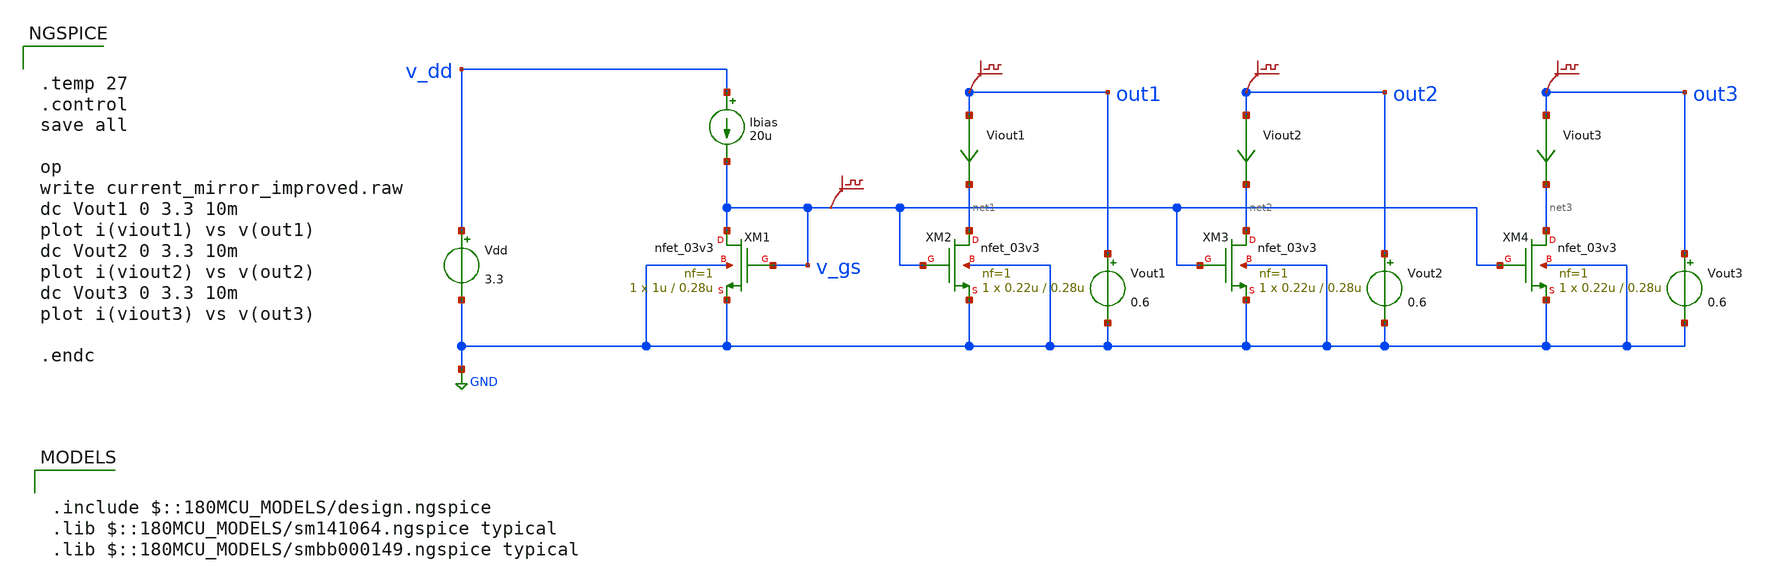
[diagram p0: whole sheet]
** sch_path: Modulo_Analogico/Laboratorios/Lab4/current_mirror_improved.sch
**.subckt current_mirror_improved
Vdd v_dd GND 3.3
Ibias v_dd v_gs 20u
Vout1 out1 GND 0.6
Vout2 out2 GND 0.6
Vout3 out3 GND 0.6
.save v(out1)
.save v(out2)
.save v(out3)
.save v(v_gs)
Viout1 out1 net1 0
.save i(viout1)
Viout2 out2 net2 0
.save i(viout2)
Viout3 out3 net3 0
.save i(viout3)
XM1 v_gs v_gs GND GND nfet_03v3 L=0.28u W=1u nf=1 ad='int((nf+1)/2) * W/nf * 0.18u' as='int((nf+2)/2) * W/nf * 0.18u'
+ pd='2*int((nf+1)/2) * (W/nf + 0.18u)' ps='2*int((nf+2)/2) * (W/nf + 0.18u)' nrd='0.18u / W' nrs='0.18u / W'
+ sa=0 sb=0 sd=0 m=1
XM2 net1 v_gs GND GND nfet_03v3 L=0.28u W=0.22u nf=1 ad='int((nf+1)/2) * W/nf * 0.18u' as='int((nf+2)/2) * W/nf * 0.18u'
+ pd='2*int((nf+1)/2) * (W/nf + 0.18u)' ps='2*int((nf+2)/2) * (W/nf + 0.18u)' nrd='0.18u / W' nrs='0.18u / W'
+ sa=0 sb=0 sd=0 m=1
XM3 net2 v_gs GND GND nfet_03v3 L=0.28u W=0.22u nf=1 ad='int((nf+1)/2) * W/nf * 0.18u' as='int((nf+2)/2) * W/nf * 0.18u'
+ pd='2*int((nf+1)/2) * (W/nf + 0.18u)' ps='2*int((nf+2)/2) * (W/nf + 0.18u)' nrd='0.18u / W' nrs='0.18u / W'
+ sa=0 sb=0 sd=0 m=1
XM4 net3 v_gs GND GND nfet_03v3 L=0.28u W=0.22u nf=1 ad='int((nf+1)/2) * W/nf * 0.18u' as='int((nf+2)/2) * W/nf * 0.18u'
+ pd='2*int((nf+1)/2) * (W/nf + 0.18u)' ps='2*int((nf+2)/2) * (W/nf + 0.18u)' nrd='0.18u / W' nrs='0.18u / W'
+ sa=0 sb=0 sd=0 m=1
**** begin user architecture code


.temp 27
.control
save all

op
write current_mirror_improved.raw
dc Vout1 0 3.3 10m
plot i(viout1) vs v(out1)
dc Vout2 0 3.3 10m
plot i(viout2) vs v(out2)
dc Vout3 0 3.3 10m
plot i(viout3) vs v(out3)

.endc



.include $::180MCU_MODELS/design.ngspice
.lib $::180MCU_MODELS/sm141064.ngspice typical
.lib $::180MCU_MODELS/smbb000149.ngspice typical

**** end user architecture code
**.ends
.GLOBAL GND
.end
